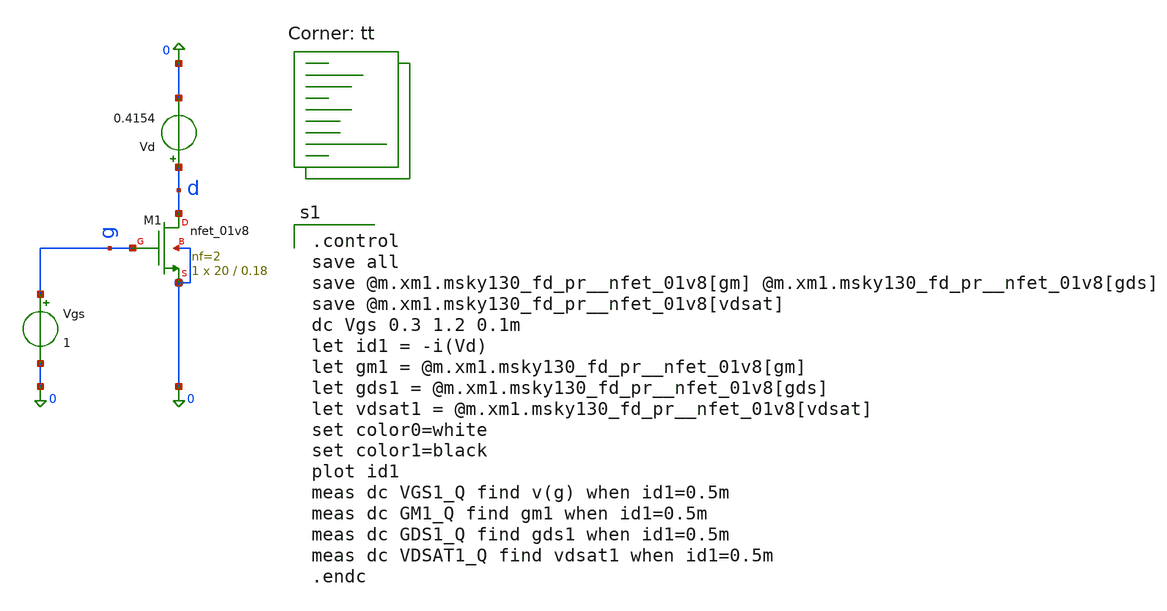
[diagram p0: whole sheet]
** sch_path: Homework 6 - Simulation on Open Source Softwares/Simulations/ex6_m1.sch
**.subckt ex6_m1
XM1 d g 0 0 sky130_fd_pr__nfet_01v8 L=0.18 W=20 nf=2 ad='int((2 + 1)/2) * 20 / 2 * 0.29' as='int((2 + 2)/2) * 20 / 2 * 0.29'
+ pd='2*int((2 + 1)/2) * (20 / 2 + 0.29)' ps='2*int((2 + 2)/2) * (20 / 2 + 0.29)' nrd='0.29 / 20 ' nrs='0.29 / 20 '
+ sa=0 sb=0 sd=0 mult=1 m=1
Vd d 0 0.4154
Vgs g 0 1
**** begin user architecture code

.control
save all
save @m.xm1.msky130_fd_pr__nfet_01v8[gm] @m.xm1.msky130_fd_pr__nfet_01v8[gds]
save @m.xm1.msky130_fd_pr__nfet_01v8[vdsat]
dc Vgs 0.3 1.2 0.1m
let id1 = -i(Vd)
let gm1 = @m.xm1.msky130_fd_pr__nfet_01v8[gm]
let gds1 = @m.xm1.msky130_fd_pr__nfet_01v8[gds]
let vdsat1 = @m.xm1.msky130_fd_pr__nfet_01v8[vdsat]
set color0=white
set color1=black
plot id1
meas dc VGS1_Q find v(g) when id1=0.5m
meas dc GM1_Q find gm1 when id1=0.5m
meas dc GDS1_Q find gds1 when id1=0.5m
meas dc VDSAT1_Q find vdsat1 when id1=0.5m
.endc

.lib $::SKYWATER_MODELS/sky130.lib.spice tt
**** end user architecture code
**.ends
.end
